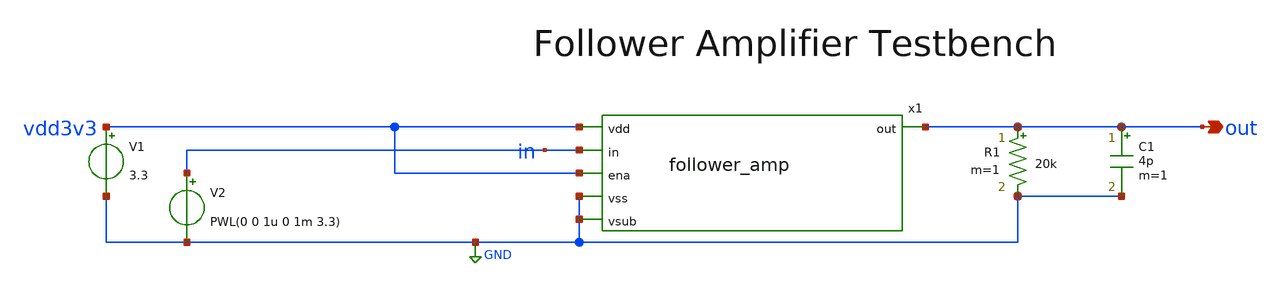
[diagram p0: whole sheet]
** sch_path: xschem/follower_amp_tb.sch
**.subckt follower_amp_tb out
*.opin out
V1 vdd3v3 GND 3.3
R1 out GND 20k m=1
V2 in GND PWL(0 0 1u 0 1m 3.3)
C1 out GND 4p m=1
x1 vdd3v3 out vdd3v3 GND in GND follower_amp
**** begin user architecture code

.lib /usr/share/pdk/sky130A/libs.tech/ngspice/sky130.lib.spice tt


.control
tran 100n 1.1m
plot V(out) V(in)
plot V(out)-V(in)
plot x1.pdrv1 x1.pdrv2 x1.ndrv
plot x1.vcomp x1.vcomn1 x1.vcomn2
.endc

**** end user architecture code
**.ends
.GLOBAL GND
.end
